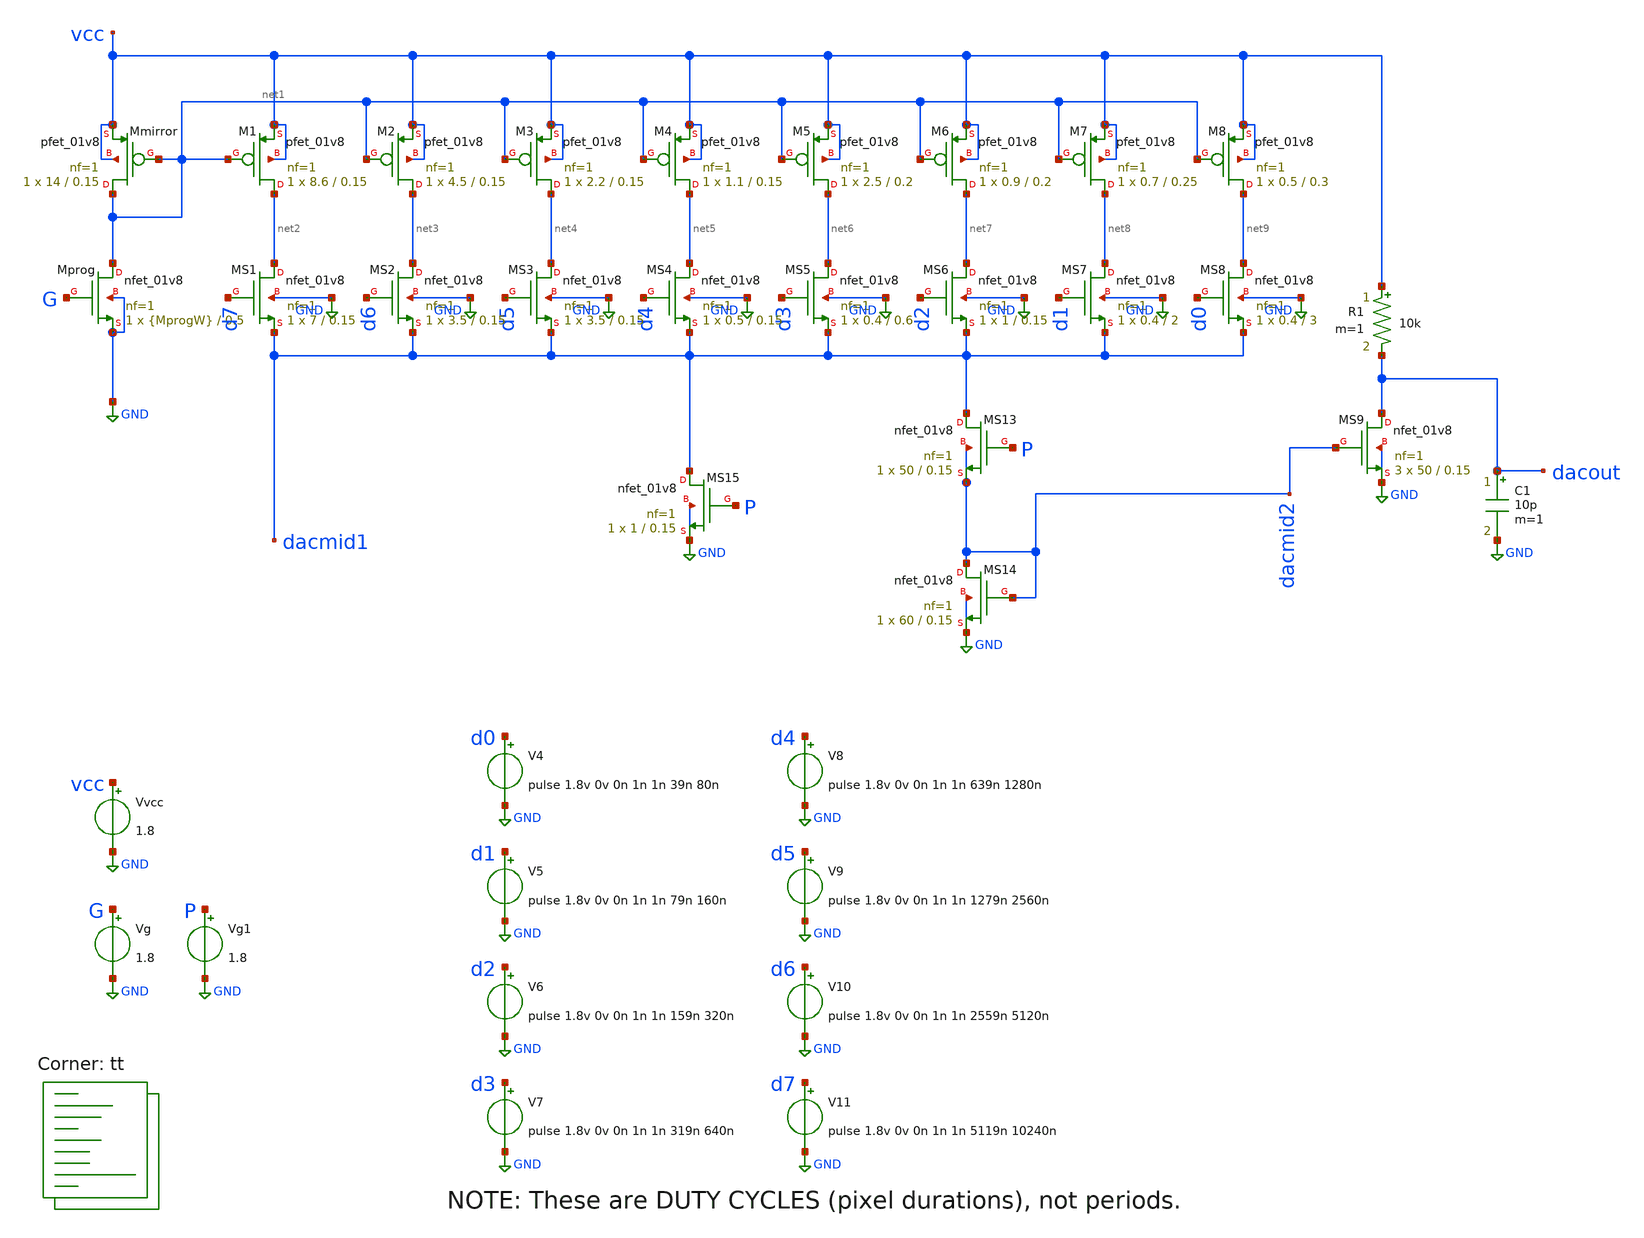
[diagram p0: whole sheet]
** sch_path: xschem/06a-sorta.sch
**.subckt 06a-sorta
Vvcc vcc GND 1.8
Vg G GND 1.8
XMprog net1 G GND GND sky130_fd_pr__nfet_01v8 L=0.5 W={MprogW} nf=1 ad='int((nf+1)/2) * W/nf * 0.29'
+ as='int((nf+2)/2) * W/nf * 0.29' pd='2*int((nf+1)/2) * (W/nf + 0.29)' ps='2*int((nf+2)/2) * (W/nf + 0.29)'
+ nrd='0.29 / W' nrs='0.29 / W' sa=0 sb=0 sd=0 mult=1 m=1
XMmirror net1 net1 vcc vcc sky130_fd_pr__pfet_01v8 L=0.15 W=14 nf=1 ad='int((nf+1)/2) * W/nf * 0.29'
+ as='int((nf+2)/2) * W/nf * 0.29' pd='2*int((nf+1)/2) * (W/nf + 0.29)' ps='2*int((nf+2)/2) * (W/nf + 0.29)'
+ nrd='0.29 / W' nrs='0.29 / W' sa=0 sb=0 sd=0 mult=1 m=1
XM1 net2 net1 vcc vcc sky130_fd_pr__pfet_01v8 L=0.15 W=8.6 nf=1 ad='int((nf+1)/2) * W/nf * 0.29' as='int((nf+2)/2) * W/nf * 0.29'
+ pd='2*int((nf+1)/2) * (W/nf + 0.29)' ps='2*int((nf+2)/2) * (W/nf + 0.29)' nrd='0.29 / W' nrs='0.29 / W'
+ sa=0 sb=0 sd=0 mult=1 m=1
XM2 net3 net1 vcc vcc sky130_fd_pr__pfet_01v8 L=0.15 W=4.5 nf=1 ad='int((nf+1)/2) * W/nf * 0.29' as='int((nf+2)/2) * W/nf * 0.29'
+ pd='2*int((nf+1)/2) * (W/nf + 0.29)' ps='2*int((nf+2)/2) * (W/nf + 0.29)' nrd='0.29 / W' nrs='0.29 / W'
+ sa=0 sb=0 sd=0 mult=1 m=1
XM3 net4 net1 vcc vcc sky130_fd_pr__pfet_01v8 L=0.15 W=2.2 nf=1 ad='int((nf+1)/2) * W/nf * 0.29' as='int((nf+2)/2) * W/nf * 0.29'
+ pd='2*int((nf+1)/2) * (W/nf + 0.29)' ps='2*int((nf+2)/2) * (W/nf + 0.29)' nrd='0.29 / W' nrs='0.29 / W'
+ sa=0 sb=0 sd=0 mult=1 m=1
XM4 net5 net1 vcc vcc sky130_fd_pr__pfet_01v8 L=0.15 W=1.1 nf=1 ad='int((nf+1)/2) * W/nf * 0.29' as='int((nf+2)/2) * W/nf * 0.29'
+ pd='2*int((nf+1)/2) * (W/nf + 0.29)' ps='2*int((nf+2)/2) * (W/nf + 0.29)' nrd='0.29 / W' nrs='0.29 / W'
+ sa=0 sb=0 sd=0 mult=1 m=1
XM5 net6 net1 vcc vcc sky130_fd_pr__pfet_01v8 L=0.2 W=2.5 nf=1 ad='int((nf+1)/2) * W/nf * 0.29' as='int((nf+2)/2) * W/nf * 0.29'
+ pd='2*int((nf+1)/2) * (W/nf + 0.29)' ps='2*int((nf+2)/2) * (W/nf + 0.29)' nrd='0.29 / W' nrs='0.29 / W'
+ sa=0 sb=0 sd=0 mult=1 m=1
XM6 net7 net1 vcc vcc sky130_fd_pr__pfet_01v8 L=0.2 W=0.9 nf=1 ad='int((nf+1)/2) * W/nf * 0.29' as='int((nf+2)/2) * W/nf * 0.29'
+ pd='2*int((nf+1)/2) * (W/nf + 0.29)' ps='2*int((nf+2)/2) * (W/nf + 0.29)' nrd='0.29 / W' nrs='0.29 / W'
+ sa=0 sb=0 sd=0 mult=1 m=1
XM7 net8 net1 vcc vcc sky130_fd_pr__pfet_01v8 L=0.25 W=0.7 nf=1 ad='int((nf+1)/2) * W/nf * 0.29' as='int((nf+2)/2) * W/nf * 0.29'
+ pd='2*int((nf+1)/2) * (W/nf + 0.29)' ps='2*int((nf+2)/2) * (W/nf + 0.29)' nrd='0.29 / W' nrs='0.29 / W'
+ sa=0 sb=0 sd=0 mult=1 m=1
XM8 net9 net1 vcc vcc sky130_fd_pr__pfet_01v8 L=0.3 W=0.5 nf=1 ad='int((nf+1)/2) * W/nf * 0.29' as='int((nf+2)/2) * W/nf * 0.29'
+ pd='2*int((nf+1)/2) * (W/nf + 0.29)' ps='2*int((nf+2)/2) * (W/nf + 0.29)' nrd='0.29 / W' nrs='0.29 / W'
+ sa=0 sb=0 sd=0 mult=1 m=1
XMS1 net2 d7 dacmid1 GND sky130_fd_pr__nfet_01v8 L=0.15 W=7 nf=1 ad='int((nf+1)/2) * W/nf * 0.29' as='int((nf+2)/2) * W/nf * 0.29'
+ pd='2*int((nf+1)/2) * (W/nf + 0.29)' ps='2*int((nf+2)/2) * (W/nf + 0.29)' nrd='0.29 / W' nrs='0.29 / W'
+ sa=0 sb=0 sd=0 mult=1 m=1
XMS2 net3 d6 dacmid1 GND sky130_fd_pr__nfet_01v8 L=0.15 W=3.5 nf=1 ad='int((nf+1)/2) * W/nf * 0.29' as='int((nf+2)/2) * W/nf * 0.29'
+ pd='2*int((nf+1)/2) * (W/nf + 0.29)' ps='2*int((nf+2)/2) * (W/nf + 0.29)' nrd='0.29 / W' nrs='0.29 / W'
+ sa=0 sb=0 sd=0 mult=1 m=1
XMS3 net4 d5 dacmid1 GND sky130_fd_pr__nfet_01v8 L=0.15 W=3.5 nf=1 ad='int((nf+1)/2) * W/nf * 0.29' as='int((nf+2)/2) * W/nf * 0.29'
+ pd='2*int((nf+1)/2) * (W/nf + 0.29)' ps='2*int((nf+2)/2) * (W/nf + 0.29)' nrd='0.29 / W' nrs='0.29 / W'
+ sa=0 sb=0 sd=0 mult=1 m=1
XMS4 net5 d4 dacmid1 GND sky130_fd_pr__nfet_01v8 L=0.15 W=0.5 nf=1 ad='int((nf+1)/2) * W/nf * 0.29' as='int((nf+2)/2) * W/nf * 0.29'
+ pd='2*int((nf+1)/2) * (W/nf + 0.29)' ps='2*int((nf+2)/2) * (W/nf + 0.29)' nrd='0.29 / W' nrs='0.29 / W'
+ sa=0 sb=0 sd=0 mult=1 m=1
XMS5 net6 d3 dacmid1 GND sky130_fd_pr__nfet_01v8 L=0.6 W=0.4 nf=1 ad='int((nf+1)/2) * W/nf * 0.29' as='int((nf+2)/2) * W/nf * 0.29'
+ pd='2*int((nf+1)/2) * (W/nf + 0.29)' ps='2*int((nf+2)/2) * (W/nf + 0.29)' nrd='0.29 / W' nrs='0.29 / W'
+ sa=0 sb=0 sd=0 mult=1 m=1
XMS6 net7 d2 dacmid1 GND sky130_fd_pr__nfet_01v8 L=0.15 W=1 nf=1 ad='int((nf+1)/2) * W/nf * 0.29' as='int((nf+2)/2) * W/nf * 0.29'
+ pd='2*int((nf+1)/2) * (W/nf + 0.29)' ps='2*int((nf+2)/2) * (W/nf + 0.29)' nrd='0.29 / W' nrs='0.29 / W'
+ sa=0 sb=0 sd=0 mult=1 m=1
XMS7 net8 d1 dacmid1 GND sky130_fd_pr__nfet_01v8 L=2 W=0.4 nf=1 ad='int((nf+1)/2) * W/nf * 0.29' as='int((nf+2)/2) * W/nf * 0.29'
+ pd='2*int((nf+1)/2) * (W/nf + 0.29)' ps='2*int((nf+2)/2) * (W/nf + 0.29)' nrd='0.29 / W' nrs='0.29 / W'
+ sa=0 sb=0 sd=0 mult=1 m=1
XMS8 net9 d0 dacmid1 GND sky130_fd_pr__nfet_01v8 L=3 W=0.4 nf=1 ad='int((nf+1)/2) * W/nf * 0.29' as='int((nf+2)/2) * W/nf * 0.29'
+ pd='2*int((nf+1)/2) * (W/nf + 0.29)' ps='2*int((nf+2)/2) * (W/nf + 0.29)' nrd='0.29 / W' nrs='0.29 / W'
+ sa=0 sb=0 sd=0 mult=1 m=1
V4 d0 GND pulse 1.8v 0v 0n 1n 1n 39n 80n
V5 d1 GND pulse 1.8v 0v 0n 1n 1n 79n 160n
V6 d2 GND pulse 1.8v 0v 0n 1n 1n 159n 320n
V7 d3 GND pulse 1.8v 0v 0n 1n 1n 319n 640n
V8 d4 GND pulse 1.8v 0v 0n 1n 1n 639n 1280n
V9 d5 GND pulse 1.8v 0v 0n 1n 1n 1279n 2560n
V10 d6 GND pulse 1.8v 0v 0n 1n 1n 2559n 5120n
V11 d7 GND pulse 1.8v 0v 0n 1n 1n 5119n 10240n
Vg1 P GND 1.8
C1 dacout GND 10p m=1
XMS13 dacmid1 P dacmid2 dacmid2 sky130_fd_pr__nfet_01v8 L=0.15 W=50 nf=1 ad='int((nf+1)/2) * W/nf * 0.29'
+ as='int((nf+2)/2) * W/nf * 0.29' pd='2*int((nf+1)/2) * (W/nf + 0.29)' ps='2*int((nf+2)/2) * (W/nf + 0.29)'
+ nrd='0.29 / W' nrs='0.29 / W' sa=0 sb=0 sd=0 mult=1 m=1
XMS9 dacout dacmid2 GND GND sky130_fd_pr__nfet_01v8 L=0.15 W=50 nf=1 ad='int((nf+1)/2) * W/nf * 0.29'
+ as='int((nf+2)/2) * W/nf * 0.29' pd='2*int((nf+1)/2) * (W/nf + 0.29)' ps='2*int((nf+2)/2) * (W/nf + 0.29)'
+ nrd='0.29 / W' nrs='0.29 / W' sa=0 sb=0 sd=0 mult=3 m=3
R1 vcc dacout 10k m=1
XMS14 dacmid2 dacmid2 GND GND sky130_fd_pr__nfet_01v8 L=0.15 W=60 nf=1 ad='int((nf+1)/2) * W/nf * 0.29'
+ as='int((nf+2)/2) * W/nf * 0.29' pd='2*int((nf+1)/2) * (W/nf + 0.29)' ps='2*int((nf+2)/2) * (W/nf + 0.29)'
+ nrd='0.29 / W' nrs='0.29 / W' sa=0 sb=0 sd=0 mult=1 m=1
XMS15 dacmid1 P GND GND sky130_fd_pr__nfet_01v8 L=0.15 W=1 nf=1 ad='int((nf+1)/2) * W/nf * 0.29' as='int((nf+2)/2) * W/nf * 0.29'
+ pd='2*int((nf+1)/2) * (W/nf + 0.29)' ps='2*int((nf+2)/2) * (W/nf + 0.29)' nrd='0.29 / W' nrs='0.29 / W'
+ sa=0 sb=0 sd=0 mult=1 m=1
**** begin user architecture code



.param MprogW=1
.options savecurrents
.control

*  set temp=90
  save all
  tran 1n 12.8u
  write 05.raw v(dacout) v(dacmid1) v(dacmid2)

  set appendwrite
  alterparam MprogW=0.9
  reset
*  *set temp=10
  tran 1n 12.8u
  write 05.raw
* v(dacout)

.endc



.lib $::SKYWATER_MODELS/sky130.lib.spice tt
**** end user architecture code
**.ends
.GLOBAL GND
.end
